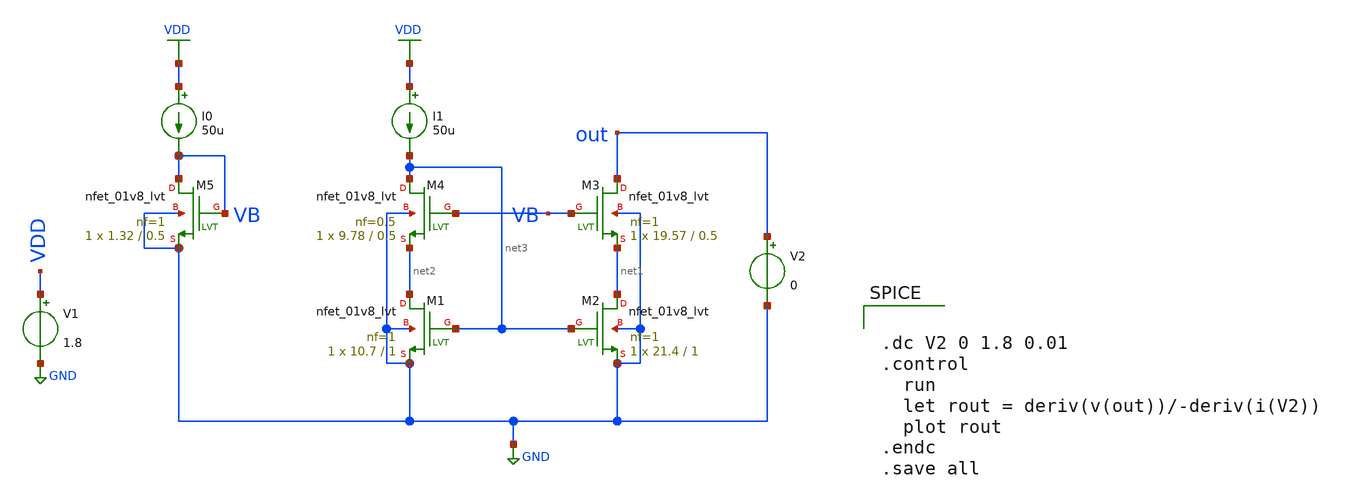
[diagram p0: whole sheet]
** sch_path: #3_LV_CM/lv_cm.sch
**.subckt lv_cm
V1 VDD GND 1.8
XM2 net1 net3 GND GND sky130_fd_pr__nfet_01v8_lvt L=1 W=21.4 nf=1 ad='int((nf+1)/2) * W/nf * 0.29' as='int((nf+2)/2) * W/nf * 0.29'
+ pd='2*int((nf+1)/2) * (W/nf + 0.29)' ps='2*int((nf+2)/2) * (W/nf + 0.29)' nrd='0.29 / W' nrs='0.29 / W'
+ sa=0 sb=0 sd=0 mult=1 m=1
XM3 out VB net1 GND sky130_fd_pr__nfet_01v8_lvt L=0.5 W=19.57 nf=1 ad='int((nf+1)/2) * W/nf * 0.29' as='int((nf+2)/2) * W/nf * 0.29'
+ pd='2*int((nf+1)/2) * (W/nf + 0.29)' ps='2*int((nf+2)/2) * (W/nf + 0.29)' nrd='0.29 / W' nrs='0.29 / W'
+ sa=0 sb=0 sd=0 mult=1 m=1
XM1 net2 net3 GND GND sky130_fd_pr__nfet_01v8_lvt L=1 W=10.7 nf=1 ad='int((nf+1)/2) * W/nf * 0.29' as='int((nf+2)/2) * W/nf * 0.29'
+ pd='2*int((nf+1)/2) * (W/nf + 0.29)' ps='2*int((nf+2)/2) * (W/nf + 0.29)' nrd='0.29 / W' nrs='0.29 / W'
+ sa=0 sb=0 sd=0 mult=1 m=1
XM5 VB VB GND GND sky130_fd_pr__nfet_01v8_lvt L=0.5 W=1.32 nf=1 ad='int((nf+1)/2) * W/nf * 0.29' as='int((nf+2)/2) * W/nf * 0.29'
+ pd='2*int((nf+1)/2) * (W/nf + 0.29)' ps='2*int((nf+2)/2) * (W/nf + 0.29)' nrd='0.29 / W' nrs='0.29 / W'
+ sa=0 sb=0 sd=0 mult=1 m=1
XM4 net3 VB net2 GND sky130_fd_pr__nfet_01v8_lvt L=0.5 W=9.78 nf=0.5 ad='int((nf+1)/2) * W/nf * 0.29'
+ as='int((nf+2)/2) * W/nf * 0.29' pd='2*int((nf+1)/2) * (W/nf + 0.29)' ps='2*int((nf+2)/2) * (W/nf + 0.29)'
+ nrd='0.29 / W' nrs='0.29 / W' sa=0 sb=0 sd=0 mult=1 m=1
V2 out GND 0
I0 VDD VB 50u
I1 VDD net3 50u
**** begin user architecture code

** opencircuitdesign pdks install
.lib $::SKYWATER_MODELS/sky130.lib.spice tt




.dc V2 0 1.8 0.01
.control
  run
  let rout = deriv(v(out))/-deriv(i(V2))
  plot rout
.endc
.save all


**** end user architecture code
**.ends
.GLOBAL GND
.GLOBAL VDD
.end
